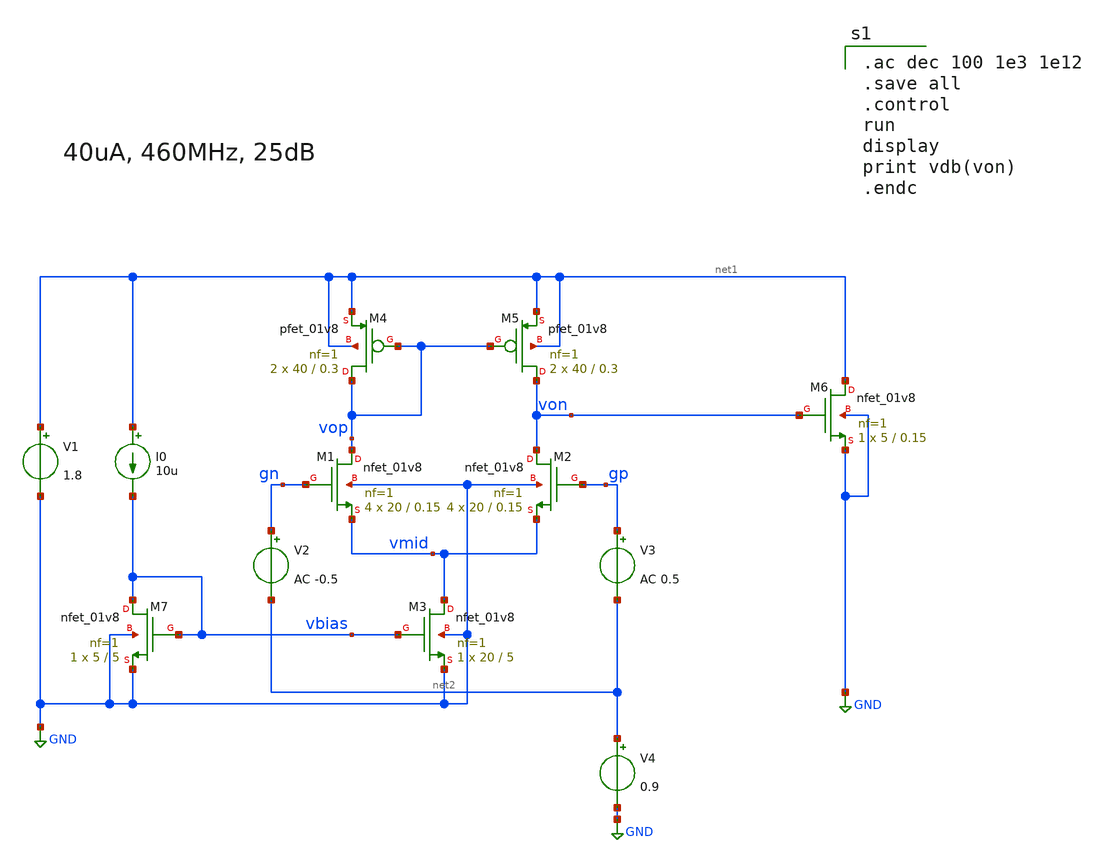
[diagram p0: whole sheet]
** sch_path: xschem/5tamp.sch
**.subckt 5tamp
XM1 vop gn vmid GND sky130_fd_pr__nfet_01v8 L=0.15 W=20 nf=1 ad='int((nf+1)/2) * W/nf * 0.29' as='int((nf+2)/2) * W/nf * 0.29'
+ pd='2*int((nf+1)/2) * (W/nf + 0.29)' ps='2*int((nf+2)/2) * (W/nf + 0.29)' nrd='0.29 / W' nrs='0.29 / W'
+ sa=0 sb=0 sd=0 mult=4 m=4
XM2 von gp vmid GND sky130_fd_pr__nfet_01v8 L=0.15 W=20 nf=1 ad='int((nf+1)/2) * W/nf * 0.29' as='int((nf+2)/2) * W/nf * 0.29'
+ pd='2*int((nf+1)/2) * (W/nf + 0.29)' ps='2*int((nf+2)/2) * (W/nf + 0.29)' nrd='0.29 / W' nrs='0.29 / W'
+ sa=0 sb=0 sd=0 mult=4 m=4
XM3 vmid vbias GND GND sky130_fd_pr__nfet_01v8 L=5 W=20 nf=1 ad='int((nf+1)/2) * W/nf * 0.29' as='int((nf+2)/2) * W/nf * 0.29'
+ pd='2*int((nf+1)/2) * (W/nf + 0.29)' ps='2*int((nf+2)/2) * (W/nf + 0.29)' nrd='0.29 / W' nrs='0.29 / W'
+ sa=0 sb=0 sd=0 mult=1 m=1
XM4 vop vop net1 net1 sky130_fd_pr__pfet_01v8 L=0.3 W=40 nf=1 ad='int((nf+1)/2) * W/nf * 0.29' as='int((nf+2)/2) * W/nf * 0.29'
+ pd='2*int((nf+1)/2) * (W/nf + 0.29)' ps='2*int((nf+2)/2) * (W/nf + 0.29)' nrd='0.29 / W' nrs='0.29 / W'
+ sa=0 sb=0 sd=0 mult=2 m=2
XM5 von vop net1 net1 sky130_fd_pr__pfet_01v8 L=0.3 W=40 nf=1 ad='int((nf+1)/2) * W/nf * 0.29' as='int((nf+2)/2) * W/nf * 0.29'
+ pd='2*int((nf+1)/2) * (W/nf + 0.29)' ps='2*int((nf+2)/2) * (W/nf + 0.29)' nrd='0.29 / W' nrs='0.29 / W'
+ sa=0 sb=0 sd=0 mult=2 m=2
V1 net1 GND 1.8
I0 net1 vbias 10u
XM7 vbias vbias GND GND sky130_fd_pr__nfet_01v8 L=5 W=5 nf=1 ad='int((nf+1)/2) * W/nf * 0.29' as='int((nf+2)/2) * W/nf * 0.29'
+ pd='2*int((nf+1)/2) * (W/nf + 0.29)' ps='2*int((nf+2)/2) * (W/nf + 0.29)' nrd='0.29 / W' nrs='0.29 / W'
+ sa=0 sb=0 sd=0 mult=1 m=1
V2 gn net2 AC -0.5
V3 gp net2 AC 0.5
V4 net2 GND 0.9
XM6 net1 von GND GND sky130_fd_pr__nfet_01v8 L=0.15 W=5 nf=1 ad='int((nf+1)/2) * W/nf * 0.29' as='int((nf+2)/2) * W/nf * 0.29'
+ pd='2*int((nf+1)/2) * (W/nf + 0.29)' ps='2*int((nf+2)/2) * (W/nf + 0.29)' nrd='0.29 / W' nrs='0.29 / W'
+ sa=0 sb=0 sd=0 mult=1 m=1
**** begin user architecture code
.lib $::SKYWATER_MODELS/sky130.lib.spice tt
.include $::PDKPATH/libs.ref/sky130_fd_sc_hvl/spice/sky130_fd_sc_hvl.spice

.ac dec 100 1e3 1e12
.save all
.control
run
display
print vdb(von)
.endc


**** end user architecture code
**.ends
.GLOBAL GND
.end
